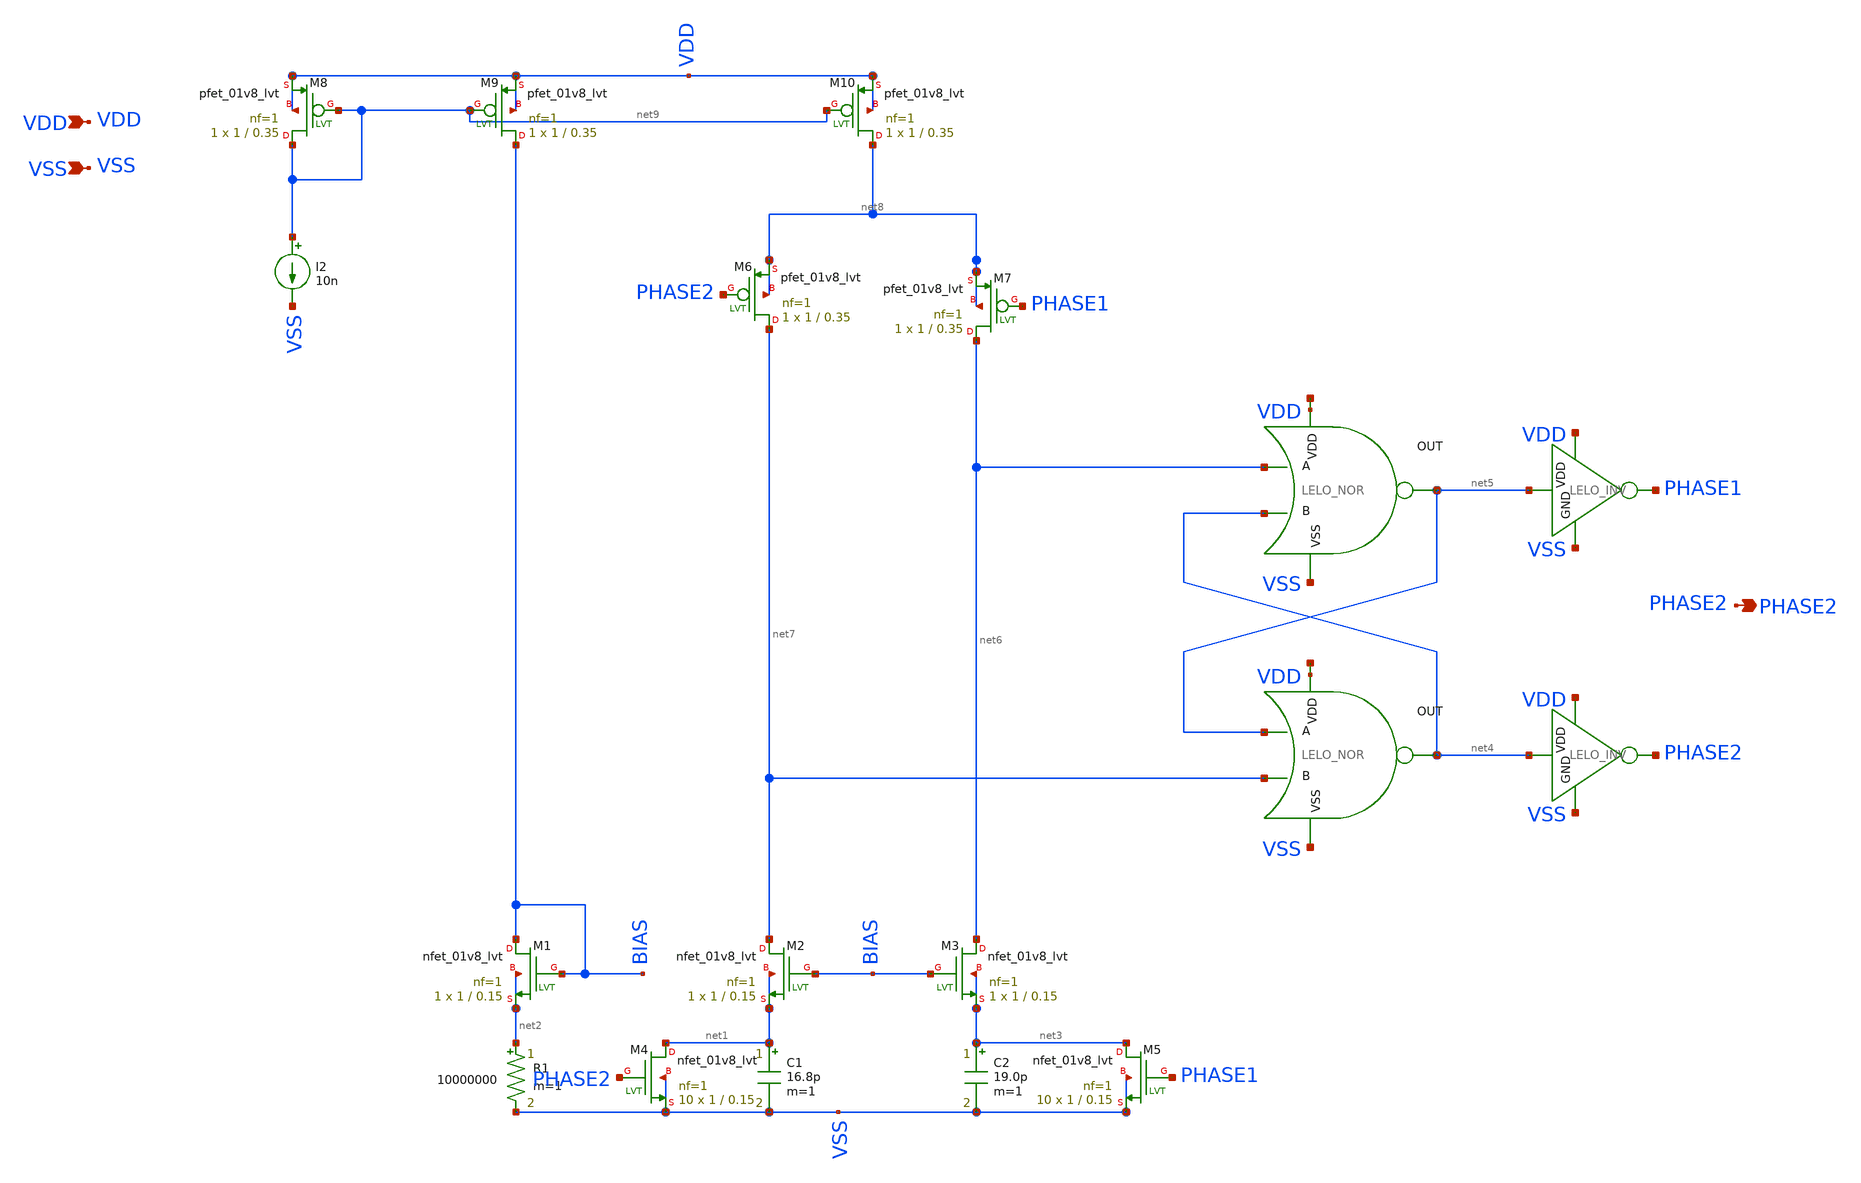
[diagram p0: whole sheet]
** sch_path: design/LELO_SVOD_SKY130A/LELO_SVOD_RELOSC_SLOW.sch
**.subckt LELO_SVOD_RELOSC_SLOW VDD VSS PHASE2
*.ipin VDD
*.ipin VSS
*.opin PHASE2
XM1 BIAS BIAS net2 net2 sky130_fd_pr__nfet_01v8_lvt L=0.15 W=1 nf=1 ad='int((1 + 1)/2) * 1 / 1 * 0.29'
+ as='int((1 + 2)/2) * 1 / 1 * 0.29' pd='2*int((1 + 1)/2) * (1 / 1 + 0.29)' ps='2*int((1 + 2)/2) * (1 / 1 + 0.29)'
+ nrd='0.29 / 1 ' nrs='0.29 / 1 ' sa=0 sb=0 sd=0 mult=1 m=1
XM2 net7 BIAS net1 net1 sky130_fd_pr__nfet_01v8_lvt L=0.15 W=1 nf=1 ad='int((1 + 1)/2) * 1 / 1 * 0.29'
+ as='int((1 + 2)/2) * 1 / 1 * 0.29' pd='2*int((1 + 1)/2) * (1 / 1 + 0.29)' ps='2*int((1 + 2)/2) * (1 / 1 + 0.29)'
+ nrd='0.29 / 1 ' nrs='0.29 / 1 ' sa=0 sb=0 sd=0 mult=1 m=1
XM3 net6 BIAS net3 net3 sky130_fd_pr__nfet_01v8_lvt L=0.15 W=1 nf=1 ad='int((1 + 1)/2) * 1 / 1 * 0.29'
+ as='int((1 + 2)/2) * 1 / 1 * 0.29' pd='2*int((1 + 1)/2) * (1 / 1 + 0.29)' ps='2*int((1 + 2)/2) * (1 / 1 + 0.29)'
+ nrd='0.29 / 1 ' nrs='0.29 / 1 ' sa=0 sb=0 sd=0 mult=1 m=1
R1 net2 VSS 10000000 m=1
C1 net1 VSS 16.8p m=1
C2 net3 VSS 19.0p m=1
XM4 net1 PHASE2 VSS VSS sky130_fd_pr__nfet_01v8_lvt L=0.15 W=1 nf=1 ad='int((1 + 1)/2) * 1 / 1 * 0.29'
+ as='int((1 + 2)/2) * 1 / 1 * 0.29' pd='2*int((1 + 1)/2) * (1 / 1 + 0.29)' ps='2*int((1 + 2)/2) * (1 / 1 + 0.29)'
+ nrd='0.29 / 1 ' nrs='0.29 / 1 ' sa=0 sb=0 sd=0 mult=10 m=10
XM5 net3 PHASE1 VSS VSS sky130_fd_pr__nfet_01v8_lvt L=0.15 W=1 nf=1 ad='int((1 + 1)/2) * 1 / 1 * 0.29'
+ as='int((1 + 2)/2) * 1 / 1 * 0.29' pd='2*int((1 + 1)/2) * (1 / 1 + 0.29)' ps='2*int((1 + 2)/2) * (1 / 1 + 0.29)'
+ nrd='0.29 / 1 ' nrs='0.29 / 1 ' sa=0 sb=0 sd=0 mult=10 m=10
x1 net10 net5 net6 net4 VSS LELO_NOR
x2 net11 net4 net5 net7 VSS LELO_NOR
XM6 net7 PHASE2 net8 net8 sky130_fd_pr__pfet_01v8_lvt L=0.35 W=1 nf=1 ad='int((1 + 1)/2) * 1 / 1 * 0.29'
+ as='int((1 + 2)/2) * 1 / 1 * 0.29' pd='2*int((1 + 1)/2) * (1 / 1 + 0.29)' ps='2*int((1 + 2)/2) * (1 / 1 + 0.29)'
+ nrd='0.29 / 1 ' nrs='0.29 / 1 ' sa=0 sb=0 sd=0 mult=1 m=1
XM7 net6 PHASE1 net8 net8 sky130_fd_pr__pfet_01v8_lvt L=0.35 W=1 nf=1 ad='int((1 + 1)/2) * 1 / 1 * 0.29'
+ as='int((1 + 2)/2) * 1 / 1 * 0.29' pd='2*int((1 + 1)/2) * (1 / 1 + 0.29)' ps='2*int((1 + 2)/2) * (1 / 1 + 0.29)'
+ nrd='0.29 / 1 ' nrs='0.29 / 1 ' sa=0 sb=0 sd=0 mult=1 m=1
x3 VDD net5 PHASE1 VSS LELO_INV
x4 VDD net4 PHASE2 VSS LELO_INV
I2 net9 VSS 10n
XM8 net9 net9 VDD VDD sky130_fd_pr__pfet_01v8_lvt L=0.35 W=1 nf=1 ad='int((1 + 1)/2) * 1 / 1 * 0.29'
+ as='int((1 + 2)/2) * 1 / 1 * 0.29' pd='2*int((1 + 1)/2) * (1 / 1 + 0.29)' ps='2*int((1 + 2)/2) * (1 / 1 + 0.29)'
+ nrd='0.29 / 1 ' nrs='0.29 / 1 ' sa=0 sb=0 sd=0 mult=1 m=1
XM9 BIAS net9 VDD VDD sky130_fd_pr__pfet_01v8_lvt L=0.35 W=1 nf=1 ad='int((1 + 1)/2) * 1 / 1 * 0.29'
+ as='int((1 + 2)/2) * 1 / 1 * 0.29' pd='2*int((1 + 1)/2) * (1 / 1 + 0.29)' ps='2*int((1 + 2)/2) * (1 / 1 + 0.29)'
+ nrd='0.29 / 1 ' nrs='0.29 / 1 ' sa=0 sb=0 sd=0 mult=1 m=1
XM10 net8 net9 VDD VDD sky130_fd_pr__pfet_01v8_lvt L=0.35 W=1 nf=1 ad='int((1 + 1)/2) * 1 / 1 * 0.29'
+ as='int((1 + 2)/2) * 1 / 1 * 0.29' pd='2*int((1 + 1)/2) * (1 / 1 + 0.29)' ps='2*int((1 + 2)/2) * (1 / 1 + 0.29)'
+ nrd='0.29 / 1 ' nrs='0.29 / 1 ' sa=0 sb=0 sd=0 mult=1 m=1
**.ends

* expanding   symbol:  LELO_SVOD_SKY130A/LELO_NOR.sym # of pins=5
** sym_path: design/LELO_SVOD_SKY130A/LELO_NOR.sym
** sch_path: design/LELO_SVOD_SKY130A/LELO_NOR.sch
.subckt LELO_NOR VDD OUT A B VSS
*.ipin VDD
*.ipin VSS
*.opin OUT
*.ipin A
*.ipin B
XM2 OUT B VSS VSS sky130_fd_pr__nfet_01v8 L=0.15 W=2 nf=1 ad='int((1 + 1)/2) * 2 / 1 * 0.29' as='int((1 + 2)/2) * 2 / 1 * 0.29'
+ pd='2*int((1 + 1)/2) * (2 / 1 + 0.29)' ps='2*int((1 + 2)/2) * (2 / 1 + 0.29)' nrd='0.29 / 2 ' nrs='0.29 / 2 '
+ sa=0 sb=0 sd=0 mult=1 m=1
XM1 OUT A VSS VSS sky130_fd_pr__nfet_01v8 L=0.15 W=2 nf=1 ad='int((1 + 1)/2) * 2 / 1 * 0.29' as='int((1 + 2)/2) * 2 / 1 * 0.29'
+ pd='2*int((1 + 1)/2) * (2 / 1 + 0.29)' ps='2*int((1 + 2)/2) * (2 / 1 + 0.29)' nrd='0.29 / 2 ' nrs='0.29 / 2 '
+ sa=0 sb=0 sd=0 mult=1 m=1
XM3 OUT B net1 VDD sky130_fd_pr__pfet_01v8 L=0.15 W=4 nf=1 ad='int((1 + 1)/2) * 4 / 1 * 0.29' as='int((1 + 2)/2) * 4 / 1 * 0.29'
+ pd='2*int((1 + 1)/2) * (4 / 1 + 0.29)' ps='2*int((1 + 2)/2) * (4 / 1 + 0.29)' nrd='0.29 / 4 ' nrs='0.29 / 4 '
+ sa=0 sb=0 sd=0 mult=1 m=1
XM4 net1 A VDD VDD sky130_fd_pr__pfet_01v8 L=0.15 W=4 nf=1 ad='int((1 + 1)/2) * 4 / 1 * 0.29' as='int((1 + 2)/2) * 4 / 1 * 0.29'
+ pd='2*int((1 + 1)/2) * (4 / 1 + 0.29)' ps='2*int((1 + 2)/2) * (4 / 1 + 0.29)' nrd='0.29 / 4 ' nrs='0.29 / 4 '
+ sa=0 sb=0 sd=0 mult=1 m=1
.ends


* expanding   symbol:  LELO_SVOD_SKY130A/LELO_INV.sym # of pins=4
** sym_path: design/LELO_SVOD_SKY130A/LELO_INV.sym
** sch_path: design/LELO_SVOD_SKY130A/LELO_INV.sch
.subckt LELO_INV VDD VIN VOUT GND
*.ipin VIN
*.ipin VDD
*.ipin GND
*.opin VOUT
XM1 VOUT VIN GND GND sky130_fd_pr__nfet_01v8_lvt L=0.15 W=1 nf=1 ad='int((1 + 1)/2) * 1 / 1 * 0.29' as='int((1 + 2)/2) * 1 / 1 * 0.29'
+ pd='2*int((1 + 1)/2) * (1 / 1 + 0.29)' ps='2*int((1 + 2)/2) * (1 / 1 + 0.29)' nrd='0.29 / 1 ' nrs='0.29 / 1 '
+ sa=0 sb=0 sd=0 mult=1 m=1
XM2 VOUT VIN VDD VDD sky130_fd_pr__pfet_01v8_lvt L=0.35 W=1 nf=1 ad='int((1 + 1)/2) * 1 / 1 * 0.29' as='int((1 + 2)/2) * 1 / 1 * 0.29'
+ pd='2*int((1 + 1)/2) * (1 / 1 + 0.29)' ps='2*int((1 + 2)/2) * (1 / 1 + 0.29)' nrd='0.29 / 1 ' nrs='0.29 / 1 '
+ sa=0 sb=0 sd=0 mult=2 m=2
.ends

.end
